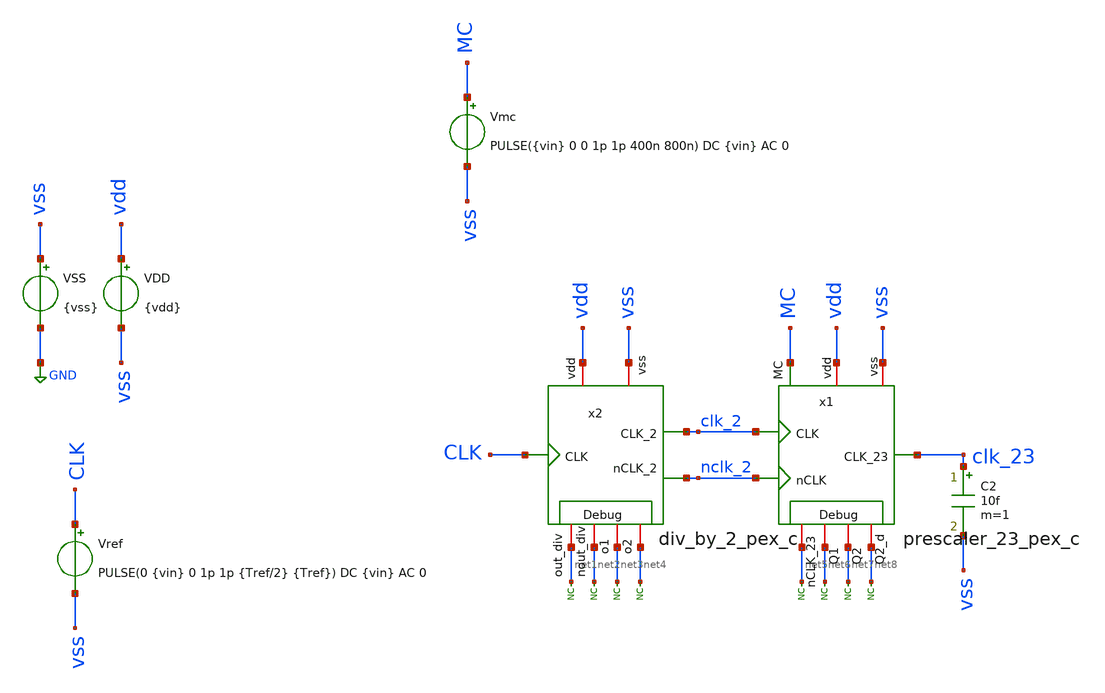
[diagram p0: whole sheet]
** sch_path: xschem/tb_prescaler_23_pex_c.sch
**.subckt tb_prescaler_23_pex_c
VSS vss GND {vss}
VDD vdd vss {vdd}
Vref CLK vss PULSE(0 {vin} 0 1p 1p {Tref/2} {Tref}) DC {vin} AC 0
C2 clk_23 vss 10f m=1
Vmc MC vss PULSE({vin} 0 0 1p 1p 400n 800n) DC {vin} AC 0
* noconn #net1
* noconn #net2
* noconn #net3
* noconn #net4
x1 vdd clk_23 clk_2 nclk_2 vss MC net6 net5 net7 net8 prescaler_23_pex_c
x2 nclk_2 vss CLK vdd clk_2 net1 net2 net3 net4 div_by_2_pex_c
* noconn #net5
* noconn #net6
* noconn #net7
* noconn #net8
**** begin user architecture code



* Parameters
.param kp = 1.0
.param vdd = kp*1.8
.param vss = 0.0
.param vin = vdd
.param fref = 1e9
.param Tref = 1/fref
.param C = 1f
.param iref=100u

.options TEMP = 100.0
.options RSHUNT = 1e20

* Models
.lib ~/skywater/skywater-pdk/libraries/sky130_fd_pr_ngspice/latest/models/corners/sky130.lib SS
.include ~/sky130-mpw2-fulgor/div_by_2/sch/simulations/div_by_2_pex_c.spice
.include ~/sky130-mpw2-fulgor/prescaler_23/sch/simulations/prescaler_23_pex_c.spice

* Data to save

.ic v(CLK) = 0.0
.ic v(MC) = 0.0
.ic v(clk_2) = 0.0
.ic v(nclk_2) = 0.0
.ic v(clk_23) = 0.0

* Simulation
.control
	save v(MC) v(CLK) v(clk_2) v(nclk_2) v(clk_23)
	tran 0.01ns 800ns
	write tb_div_by_5_tran.raw
	plot v(clk_23) v(clk) v(clk_2) v(MC)+3 v(clk_23)+6 v(clk_2)+9 v(clk)+12

.endc

.end


**** end user architecture code
**.ends
.GLOBAL GND
**** begin user architecture code
[sky130_models]
**** end user architecture code
.end
